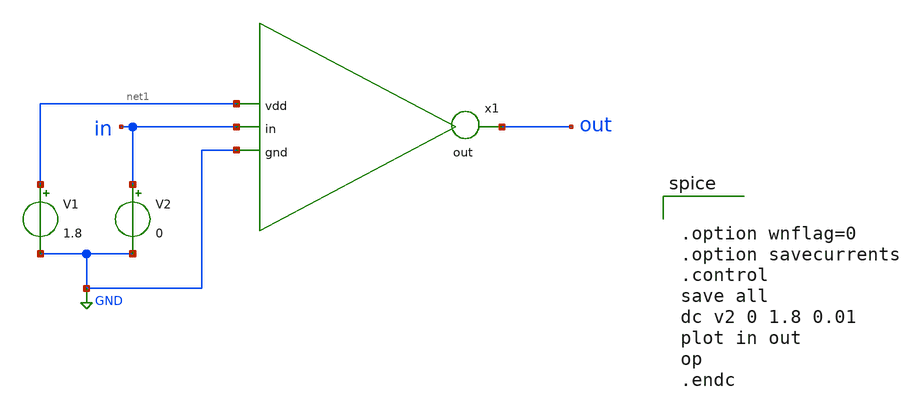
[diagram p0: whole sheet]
** sch_path: Inverter/inverter_tb.sch
**.subckt inverter_tb
V1 net1 GND 1.8
V2 in GND 0
x1 net1 out in GND inverter
**** begin user architecture code


.option wnflag=0
.option savecurrents
.control
save all
dc v2 0 1.8 0.01
plot in out
op
.endc



** opencircuitdesign pdks install
.lib $::SKYWATER_MODELS/sky130.lib.spice tt

**** end user architecture code
**.ends
.GLOBAL GND
.end
